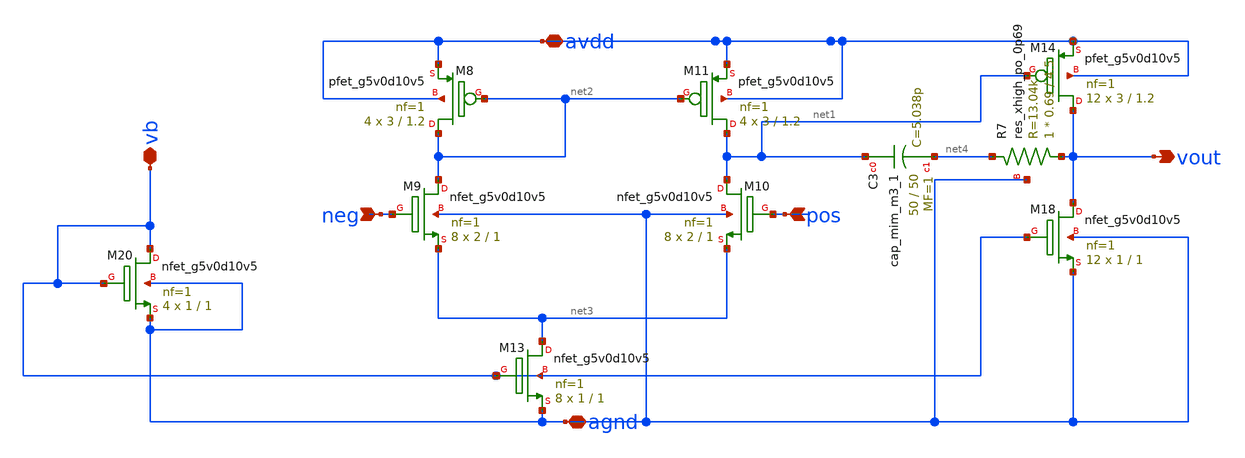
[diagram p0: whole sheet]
** sch_path: DCDC_LDO_sim/Error_Amp.sch
**.subckt Error_Amp avdd agnd vb neg pos vout
*.iopin avdd
*.iopin agnd
*.iopin vb
*.ipin neg
*.ipin pos
*.opin vout
XM8 net2 net2 avdd avdd sky130_fd_pr__pfet_g5v0d10v5 L=1.2 W=3 nf=1 ad='int((nf+1)/2) * W/nf * 0.29'
+ as='int((nf+2)/2) * W/nf * 0.29' pd='2*int((nf+1)/2) * (W/nf + 0.29)' ps='2*int((nf+2)/2) * (W/nf + 0.29)'
+ nrd='0.29 / W' nrs='0.29 / W' sa=0 sb=0 sd=0 mult=4 m=4
XM9 net2 neg net3 agnd sky130_fd_pr__nfet_g5v0d10v5 L=1 W=2 nf=1 ad='int((nf+1)/2) * W/nf * 0.29' as='int((nf+2)/2) * W/nf * 0.29'
+ pd='2*int((nf+1)/2) * (W/nf + 0.29)' ps='2*int((nf+2)/2) * (W/nf + 0.29)' nrd='0.29 / W' nrs='0.29 / W'
+ sa=0 sb=0 sd=0 mult=8 m=8
XM10 net1 pos net3 agnd sky130_fd_pr__nfet_g5v0d10v5 L=1 W=2 nf=1 ad='int((nf+1)/2) * W/nf * 0.29' as='int((nf+2)/2) * W/nf * 0.29'
+ pd='2*int((nf+1)/2) * (W/nf + 0.29)' ps='2*int((nf+2)/2) * (W/nf + 0.29)' nrd='0.29 / W' nrs='0.29 / W'
+ sa=0 sb=0 sd=0 mult=8 m=8
XM11 net1 net2 avdd avdd sky130_fd_pr__pfet_g5v0d10v5 L=1.2 W=3 nf=1 ad='int((nf+1)/2) * W/nf * 0.29'
+ as='int((nf+2)/2) * W/nf * 0.29' pd='2*int((nf+1)/2) * (W/nf + 0.29)' ps='2*int((nf+2)/2) * (W/nf + 0.29)'
+ nrd='0.29 / W' nrs='0.29 / W' sa=0 sb=0 sd=0 mult=4 m=4
XM13 net3 vb agnd vb sky130_fd_pr__nfet_g5v0d10v5 L=1 W=1 nf=1 ad='int((nf+1)/2) * W/nf * 0.29' as='int((nf+2)/2) * W/nf * 0.29'
+ pd='2*int((nf+1)/2) * (W/nf + 0.29)' ps='2*int((nf+2)/2) * (W/nf + 0.29)' nrd='0.29 / W' nrs='0.29 / W'
+ sa=0 sb=0 sd=0 mult=8 m=8
XM14 vout net1 avdd avdd sky130_fd_pr__pfet_g5v0d10v5 L=1.2 W=3 nf=1 ad='int((nf+1)/2) * W/nf * 0.29'
+ as='int((nf+2)/2) * W/nf * 0.29' pd='2*int((nf+1)/2) * (W/nf + 0.29)' ps='2*int((nf+2)/2) * (W/nf + 0.29)'
+ nrd='0.29 / W' nrs='0.29 / W' sa=0 sb=0 sd=0 mult=12 m=12
XM18 vout vb agnd agnd sky130_fd_pr__nfet_g5v0d10v5 L=1 W=1 nf=1 ad='int((nf+1)/2) * W/nf * 0.29' as='int((nf+2)/2) * W/nf * 0.29'
+ pd='2*int((nf+1)/2) * (W/nf + 0.29)' ps='2*int((nf+2)/2) * (W/nf + 0.29)' nrd='0.29 / W' nrs='0.29 / W'
+ sa=0 sb=0 sd=0 mult=12 m=12
XC3 net1 net4 sky130_fd_pr__cap_mim_m3_1 W=50 L=50 MF=1 m=1
XR7 vout net4 agnd sky130_fd_pr__res_xhigh_po_0p69 L=4.5 mult=1 m=1
XM20 vb vb agnd agnd sky130_fd_pr__nfet_g5v0d10v5 L=1 W=1 nf=1 ad='int((nf+1)/2) * W/nf * 0.29' as='int((nf+2)/2) * W/nf * 0.29'
+ pd='2*int((nf+1)/2) * (W/nf + 0.29)' ps='2*int((nf+2)/2) * (W/nf + 0.29)' nrd='0.29 / W' nrs='0.29 / W'
+ sa=0 sb=0 sd=0 mult=4 m=4
**.ends
.end
